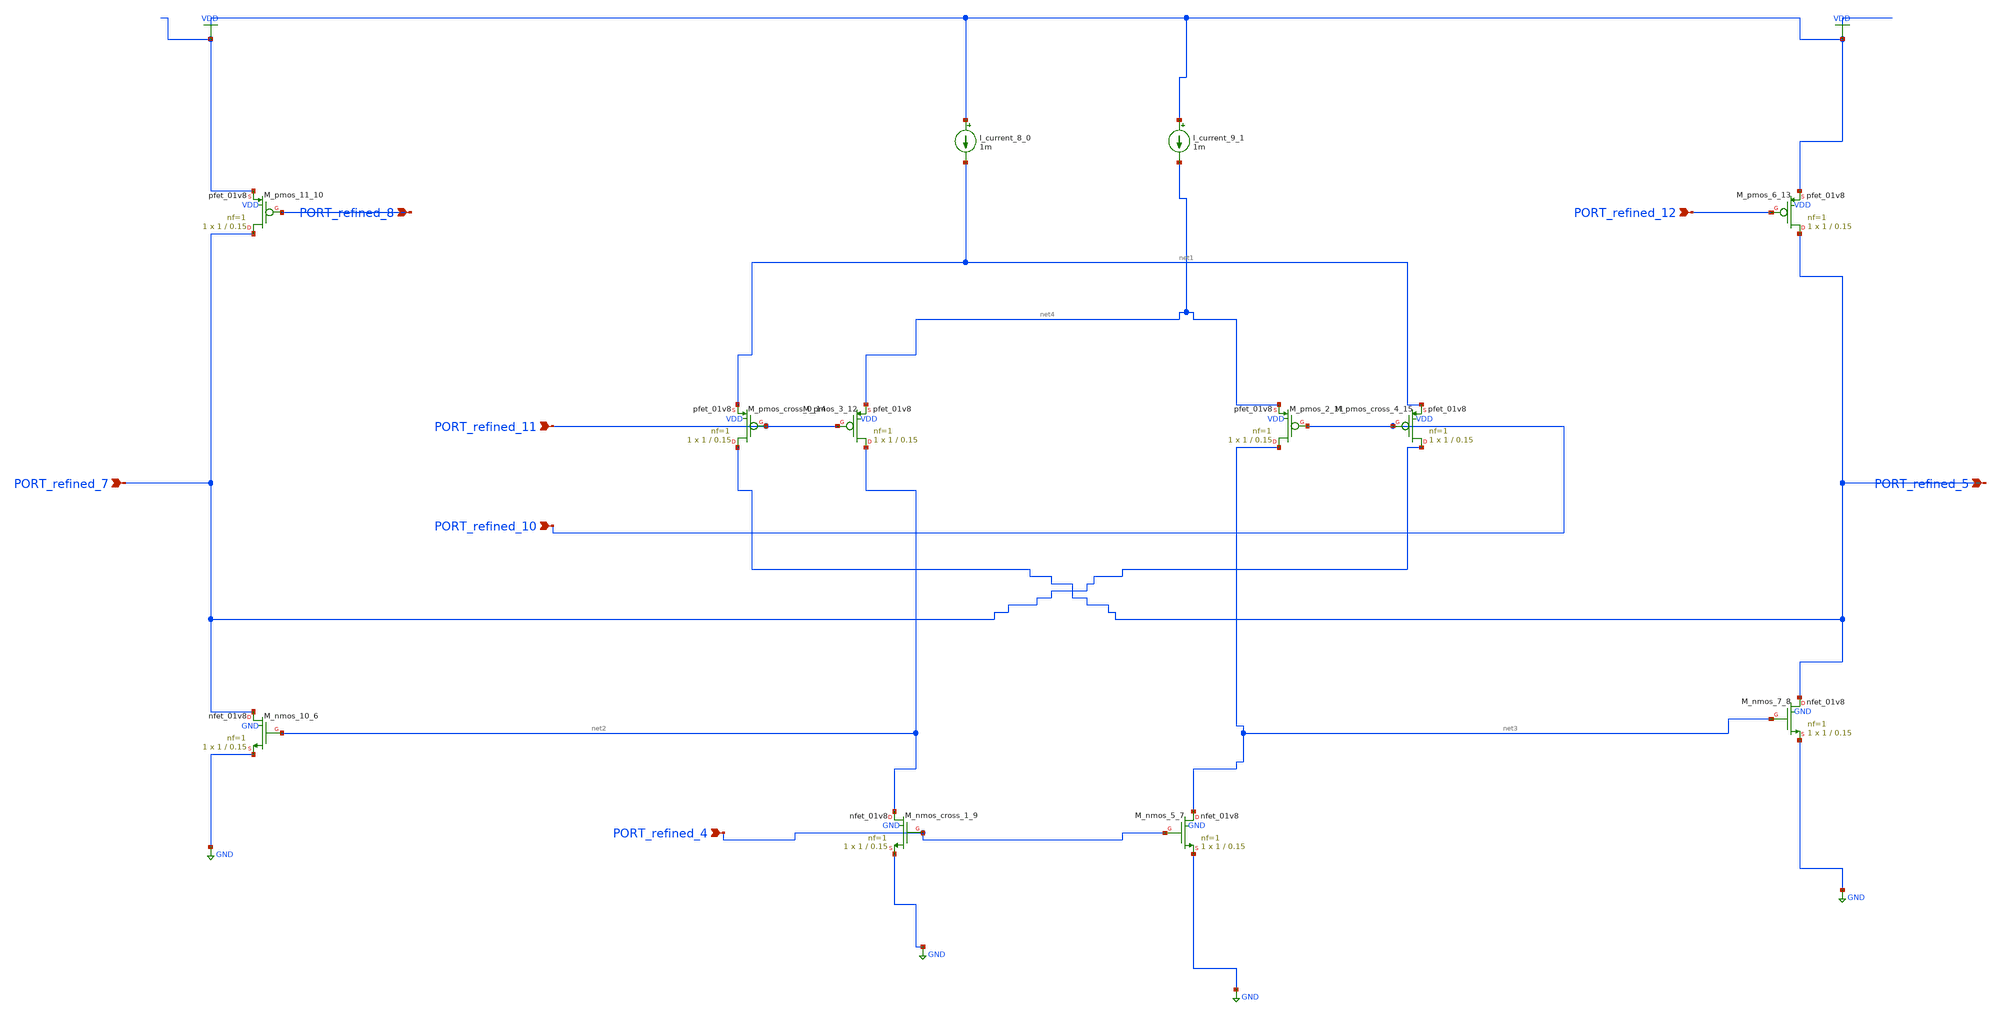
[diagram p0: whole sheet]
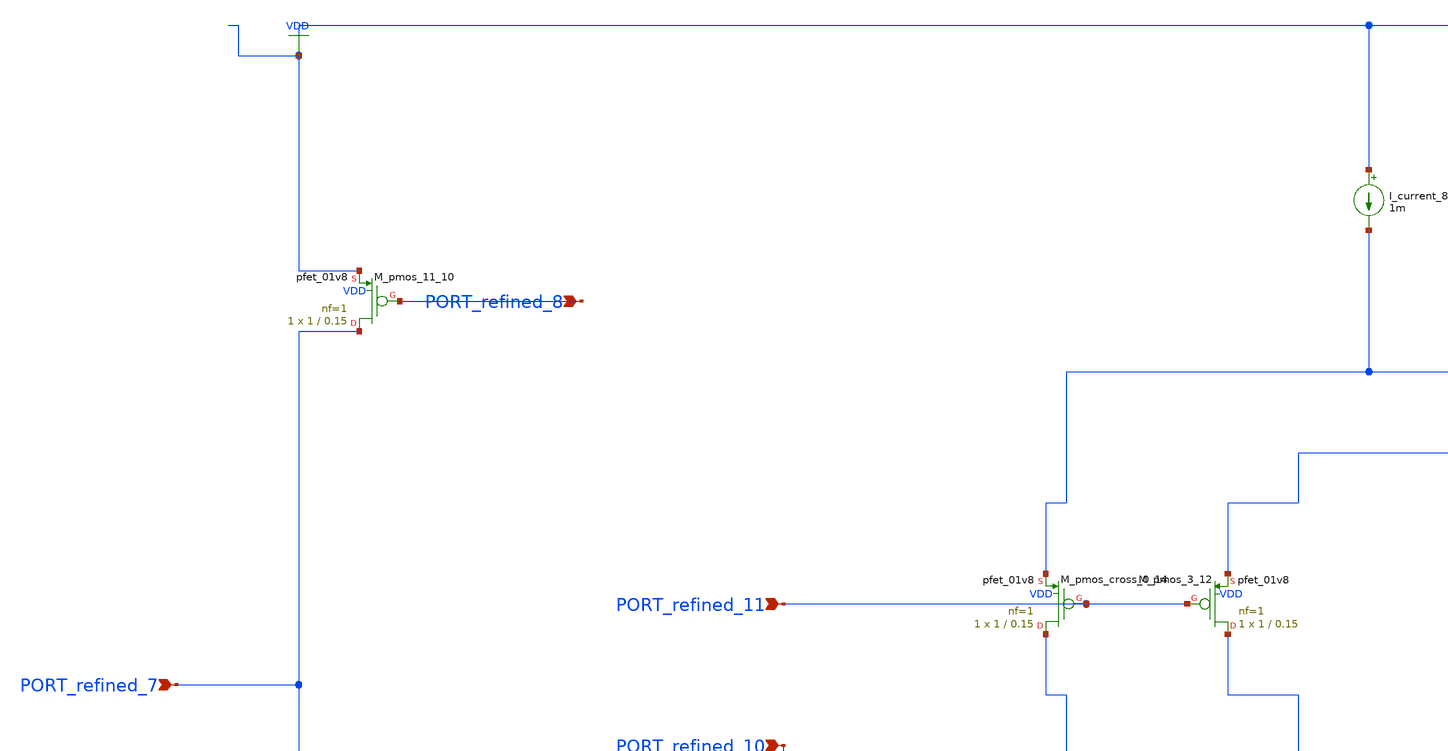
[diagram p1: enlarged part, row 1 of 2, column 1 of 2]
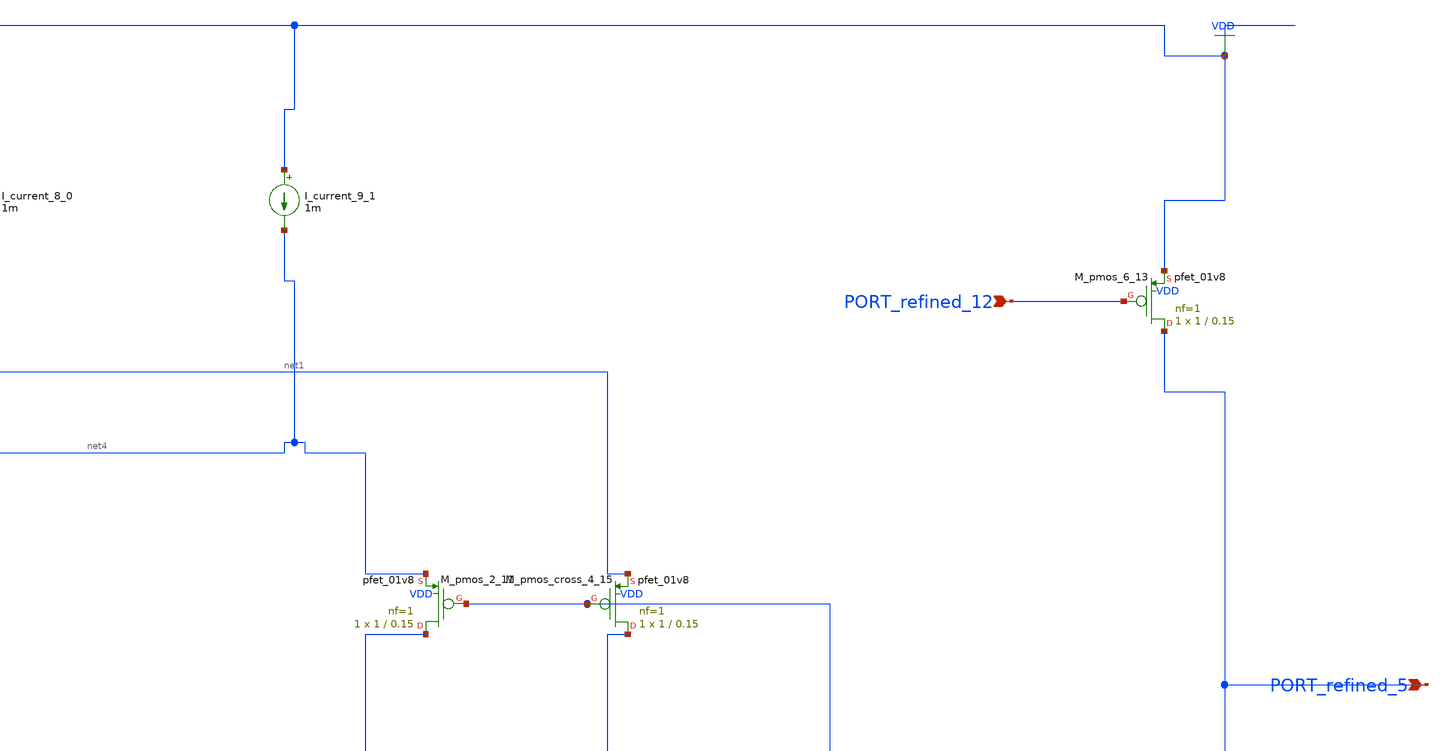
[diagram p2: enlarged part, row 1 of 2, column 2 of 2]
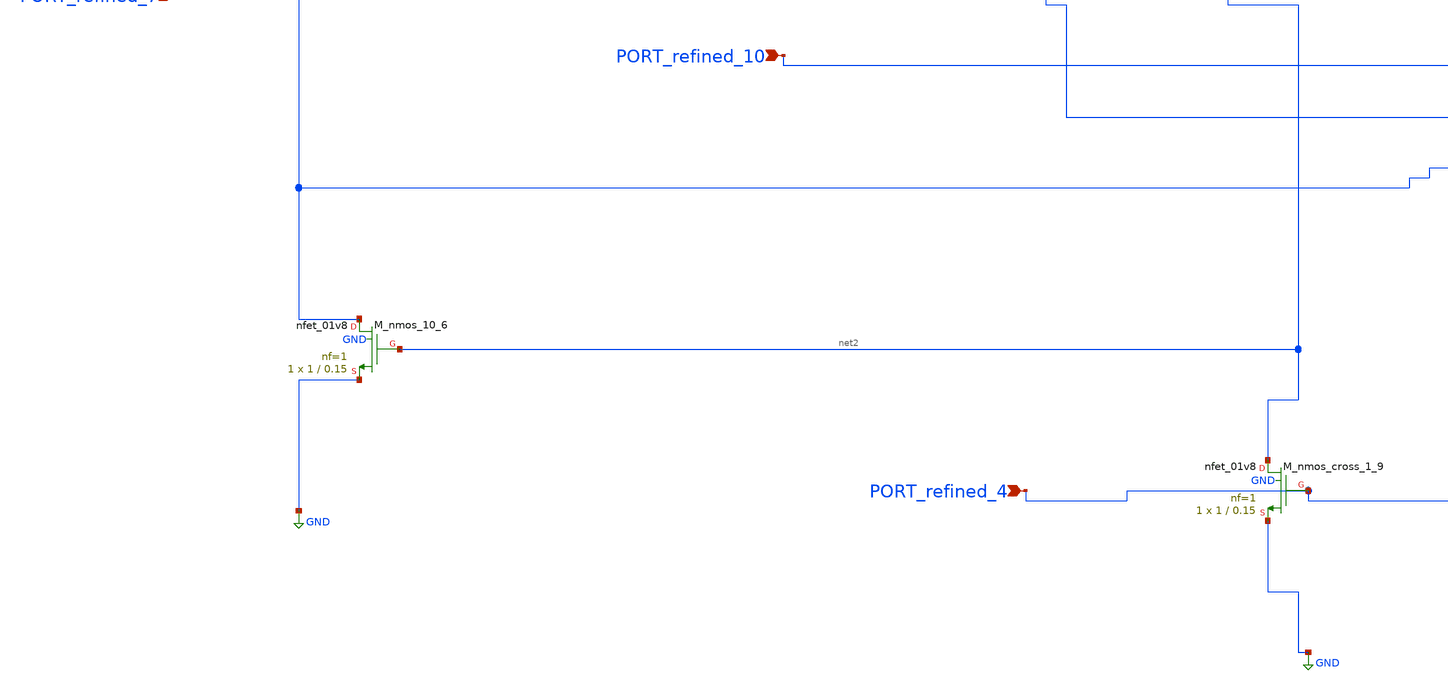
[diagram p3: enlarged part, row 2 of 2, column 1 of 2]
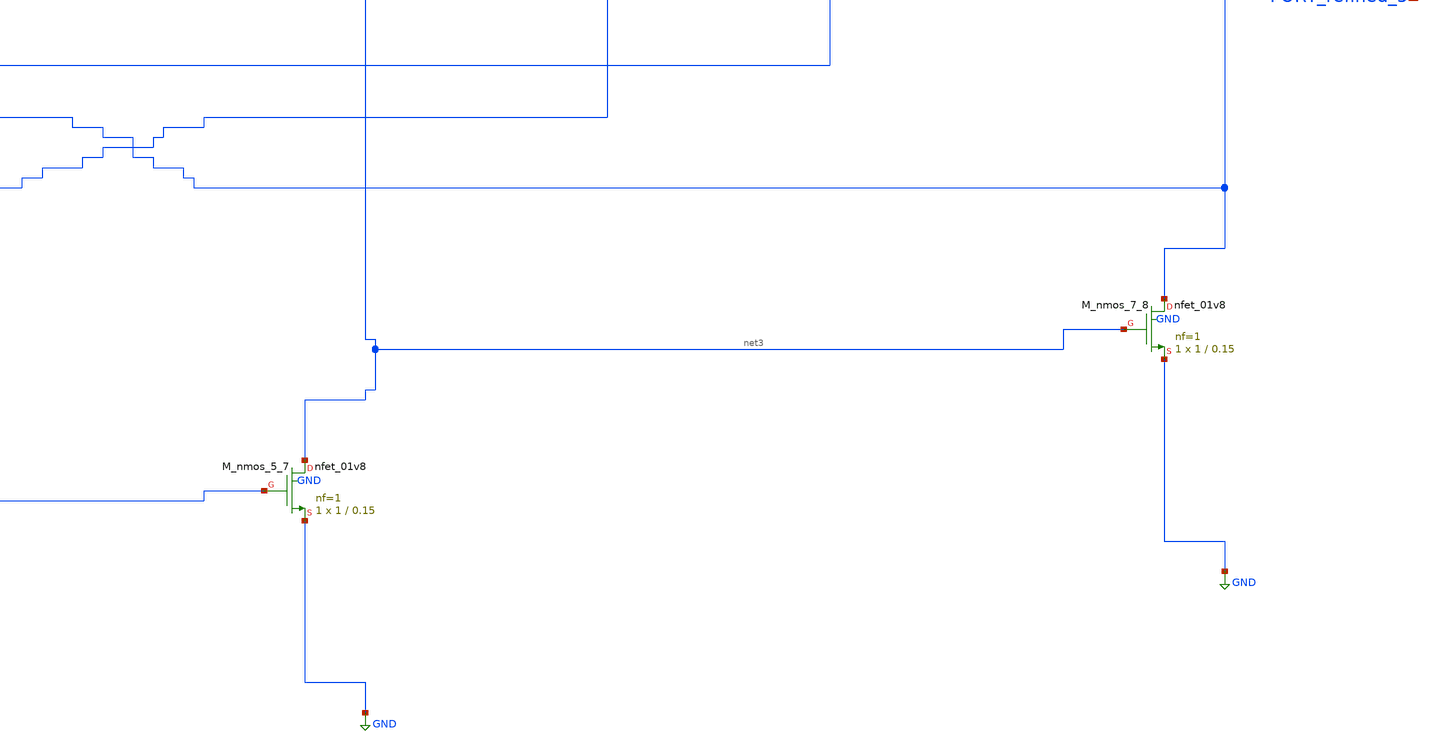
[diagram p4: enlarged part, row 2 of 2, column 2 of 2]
** sch_path: schematics/AMSNet/717.sch
**.subckt 717 PORT_refined_10 PORT_refined_5 PORT_refined_11 PORT_refined_7 PORT_refined_12
*+ PORT_refined_8 PORT_refined_4
*.ipin PORT_refined_10
*.ipin PORT_refined_5
*.ipin PORT_refined_11
*.ipin PORT_refined_7
*.ipin PORT_refined_12
*.ipin PORT_refined_8
*.ipin PORT_refined_4
I_current_8_0 VDD net1 1m
I_current_9_1 VDD net4 1m
XM_nmos_10_6 PORT_refined_7 net2 GND GND sky130_fd_pr__nfet_01v8 L=0.15 W=1 nf=1 ad='int((1 + 1)/2) * 1 / 1 * 0.29'
+ as='int((1 + 2)/2) * 1 / 1 * 0.29' pd='2*int((1 + 1)/2) * (1 / 1 + 0.29)' ps='2*int((1 + 2)/2) * (1 / 1 + 0.29)'
+ nrd='0.29 / 1 ' nrs='0.29 / 1 ' sa=0 sb=0 sd=0 mult=1 m=1
XM_nmos_5_7 net3 PORT_refined_4 GND GND sky130_fd_pr__nfet_01v8 L=0.15 W=1 nf=1 ad='int((1 + 1)/2) * 1 / 1 * 0.29'
+ as='int((1 + 2)/2) * 1 / 1 * 0.29' pd='2*int((1 + 1)/2) * (1 / 1 + 0.29)' ps='2*int((1 + 2)/2) * (1 / 1 + 0.29)'
+ nrd='0.29 / 1 ' nrs='0.29 / 1 ' sa=0 sb=0 sd=0 mult=1 m=1
XM_nmos_7_8 PORT_refined_5 net3 GND GND sky130_fd_pr__nfet_01v8 L=0.15 W=1 nf=1 ad='int((1 + 1)/2) * 1 / 1 * 0.29'
+ as='int((1 + 2)/2) * 1 / 1 * 0.29' pd='2*int((1 + 1)/2) * (1 / 1 + 0.29)' ps='2*int((1 + 2)/2) * (1 / 1 + 0.29)'
+ nrd='0.29 / 1 ' nrs='0.29 / 1 ' sa=0 sb=0 sd=0 mult=1 m=1
XM_nmos_cross_1_9 net2 PORT_refined_4 GND GND sky130_fd_pr__nfet_01v8 L=0.15 W=1 nf=1 ad='int((1 + 1)/2) * 1 / 1 * 0.29'
+ as='int((1 + 2)/2) * 1 / 1 * 0.29' pd='2*int((1 + 1)/2) * (1 / 1 + 0.29)' ps='2*int((1 + 2)/2) * (1 / 1 + 0.29)'
+ nrd='0.29 / 1 ' nrs='0.29 / 1 ' sa=0 sb=0 sd=0 mult=1 m=1
XM_pmos_11_10 PORT_refined_7 PORT_refined_8 VDD VDD sky130_fd_pr__pfet_01v8 L=0.15 W=1 nf=1 ad='int((1 + 1)/2) * 1 / 1 * 0.29'
+ as='int((1 + 2)/2) * 1 / 1 * 0.29' pd='2*int((1 + 1)/2) * (1 / 1 + 0.29)' ps='2*int((1 + 2)/2) * (1 / 1 + 0.29)'
+ nrd='0.29 / 1 ' nrs='0.29 / 1 ' sa=0 sb=0 sd=0 mult=1 m=1
XM_pmos_2_11 net3 PORT_refined_10 net4 VDD sky130_fd_pr__pfet_01v8 L=0.15 W=1 nf=1 ad='int((1 + 1)/2) * 1 / 1 * 0.29'
+ as='int((1 + 2)/2) * 1 / 1 * 0.29' pd='2*int((1 + 1)/2) * (1 / 1 + 0.29)' ps='2*int((1 + 2)/2) * (1 / 1 + 0.29)'
+ nrd='0.29 / 1 ' nrs='0.29 / 1 ' sa=0 sb=0 sd=0 mult=1 m=1
XM_pmos_3_12 net2 PORT_refined_11 net4 VDD sky130_fd_pr__pfet_01v8 L=0.15 W=1 nf=1 ad='int((1 + 1)/2) * 1 / 1 * 0.29'
+ as='int((1 + 2)/2) * 1 / 1 * 0.29' pd='2*int((1 + 1)/2) * (1 / 1 + 0.29)' ps='2*int((1 + 2)/2) * (1 / 1 + 0.29)'
+ nrd='0.29 / 1 ' nrs='0.29 / 1 ' sa=0 sb=0 sd=0 mult=1 m=1
XM_pmos_6_13 PORT_refined_5 PORT_refined_12 VDD VDD sky130_fd_pr__pfet_01v8 L=0.15 W=1 nf=1 ad='int((1 + 1)/2) * 1 / 1 * 0.29'
+ as='int((1 + 2)/2) * 1 / 1 * 0.29' pd='2*int((1 + 1)/2) * (1 / 1 + 0.29)' ps='2*int((1 + 2)/2) * (1 / 1 + 0.29)'
+ nrd='0.29 / 1 ' nrs='0.29 / 1 ' sa=0 sb=0 sd=0 mult=1 m=1
XM_pmos_cross_0_14 PORT_refined_5 PORT_refined_11 net1 VDD sky130_fd_pr__pfet_01v8 L=0.15 W=1 nf=1 ad='int((1 + 1)/2) * 1 / 1 * 0.29'
+ as='int((1 + 2)/2) * 1 / 1 * 0.29' pd='2*int((1 + 1)/2) * (1 / 1 + 0.29)' ps='2*int((1 + 2)/2) * (1 / 1 + 0.29)'
+ nrd='0.29 / 1 ' nrs='0.29 / 1 ' sa=0 sb=0 sd=0 mult=1 m=1
XM_pmos_cross_4_15 PORT_refined_7 PORT_refined_10 net1 VDD sky130_fd_pr__pfet_01v8 L=0.15 W=1 nf=1 ad='int((1 + 1)/2) * 1 / 1 * 0.29'
+ as='int((1 + 2)/2) * 1 / 1 * 0.29' pd='2*int((1 + 1)/2) * (1 / 1 + 0.29)' ps='2*int((1 + 2)/2) * (1 / 1 + 0.29)'
+ nrd='0.29 / 1 ' nrs='0.29 / 1 ' sa=0 sb=0 sd=0 mult=1 m=1
**.ends
.GLOBAL GND
.GLOBAL VDD
.end
